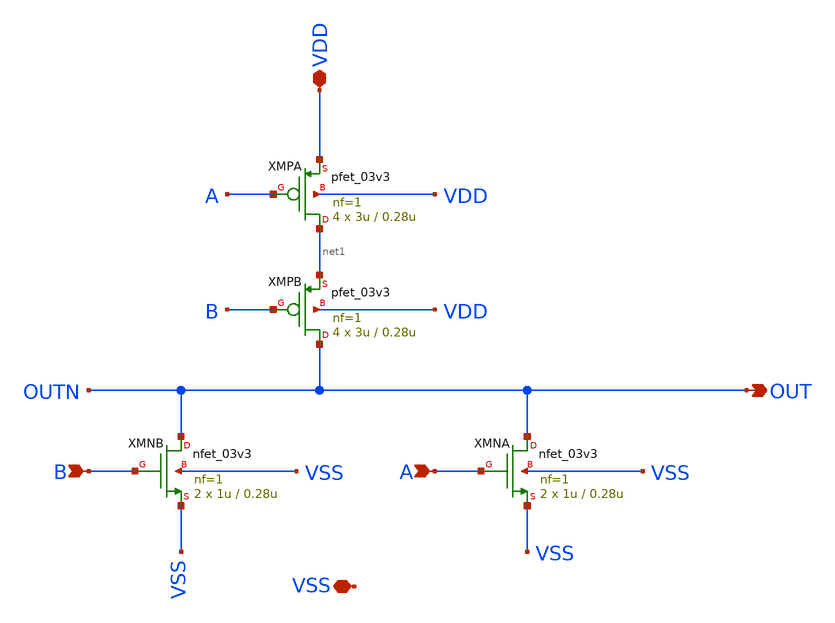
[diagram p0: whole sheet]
** sch_path: designs/DS_modulator/gate_nor/xschem/gate_nor.sch
**.subckt gate_nor OUT A VDD B VSS
*.opin OUT
*.ipin A
*.iopin VDD
*.ipin B
*.iopin VSS
XMNB OUT B VSS VSS nfet_03v3 L=0.28u W=1u nf=1 ad='int((nf+1)/2) * W/nf * 0.18u' as='int((nf+2)/2) * W/nf * 0.18u'
+ pd='2*int((nf+1)/2) * (W/nf + 0.18u)' ps='2*int((nf+2)/2) * (W/nf + 0.18u)' nrd='0.18u / W' nrs='0.18u / W'
+ sa=0 sb=0 sd=0 m=2
XMPB OUT B net1 VDD pfet_03v3 L=0.28u W=3u nf=1 ad='int((nf+1)/2) * W/nf * 0.18u' as='int((nf+2)/2) * W/nf * 0.18u'
+ pd='2*int((nf+1)/2) * (W/nf + 0.18u)' ps='2*int((nf+2)/2) * (W/nf + 0.18u)' nrd='0.18u / W' nrs='0.18u / W'
+ sa=0 sb=0 sd=0 m=4
XMNA OUT A VSS VSS nfet_03v3 L=0.28u W=1u nf=1 ad='int((nf+1)/2) * W/nf * 0.18u' as='int((nf+2)/2) * W/nf * 0.18u'
+ pd='2*int((nf+1)/2) * (W/nf + 0.18u)' ps='2*int((nf+2)/2) * (W/nf + 0.18u)' nrd='0.18u / W' nrs='0.18u / W'
+ sa=0 sb=0 sd=0 m=2
XMPA net1 A VDD VDD pfet_03v3 L=0.28u W=3u nf=1 ad='int((nf+1)/2) * W/nf * 0.18u' as='int((nf+2)/2) * W/nf * 0.18u'
+ pd='2*int((nf+1)/2) * (W/nf + 0.18u)' ps='2*int((nf+2)/2) * (W/nf + 0.18u)' nrd='0.18u / W' nrs='0.18u / W'
+ sa=0 sb=0 sd=0 m=4
**.ends
.end
